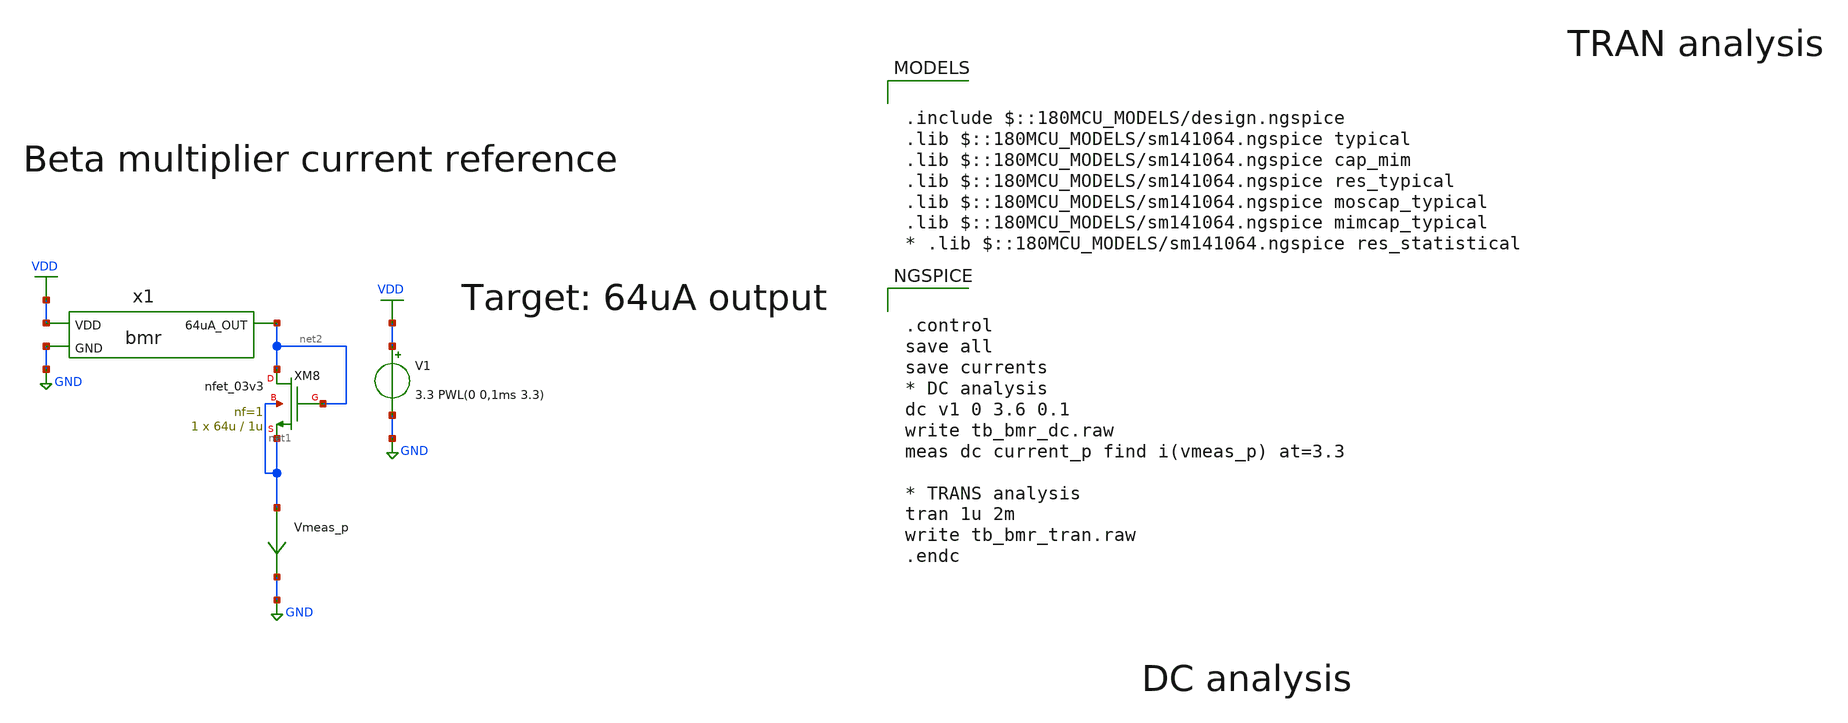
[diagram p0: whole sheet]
** sch_path: designs/libs/tb_analog/tb_bmr/tb_bmr.sch
* Copyright 2022 GlobalFoundries PDK Authors
* Licensed under the Apache License, Version 2.0 (the "License");
* you may not use this file except in compliance with the License.
* You may obtain a copy of the License at
* https://www.apache.org/licenses/LICENSE-2.0
* Unless required by applicable law or agreed to in writing, software
* distributed under the License is distributed on an "AS IS" BASIS,
* WITHOUT WARRANTIES OR CONDITIONS OF ANY KIND, either express or implied.
* See the License for the specific language governing permissions and
* limitations under the License.
**.subckt tb_bmr
V1 VDD GND 3.3 PWL(0 0,1ms 3.3)
Vmeas_p net1 GND 0
.save i(vmeas_p)
x1 VDD GND net2 bmr
XM8 net2 net2 net1 net1 nfet_03v3 L=1u W=64u nf=1 ad='int((nf+1)/2) * W/nf * 0.18u' as='int((nf+2)/2) * W/nf * 0.18u'
+ pd='2*int((nf+1)/2) * (W/nf + 0.18u)' ps='2*int((nf+2)/2) * (W/nf + 0.18u)' nrd='0.18u / W' nrs='0.18u / W'
+ sa=0 sb=0 sd=0 m=1
**** begin user architecture code


.control
save all
save currents
* DC analysis
dc v1 0 3.6 0.1
write tb_bmr_dc.raw
meas dc current_p find i(vmeas_p) at=3.3

* TRANS analysis
tran 1u 2m
write tb_bmr_tran.raw
.endc



.include $::180MCU_MODELS/design.ngspice
.lib $::180MCU_MODELS/sm141064.ngspice typical
.lib $::180MCU_MODELS/sm141064.ngspice cap_mim
.lib $::180MCU_MODELS/sm141064.ngspice res_typical
.lib $::180MCU_MODELS/sm141064.ngspice moscap_typical
.lib $::180MCU_MODELS/sm141064.ngspice mimcap_typical
* .lib $::180MCU_MODELS/sm141064.ngspice res_statistical

**** end user architecture code
**.ends

* expanding   symbol:  libs/core_analog/bmr/bmr.sym # of pins=3
** sym_path: designs/libs/core_analog/bmr/bmr.sym
** sch_path: designs/libs/core_analog/bmr/bmr.sch
.subckt bmr VDD GND 64uA_OUT
*.ipin VDD
*.ipin GND
*.opin 64uA_OUT
XM3 net2 net1 net3 GND nfet_03v3 L=1u W=10u nf=1 ad='int((nf+1)/2) * W/nf * 0.18u' as='int((nf+2)/2) * W/nf * 0.18u'
+ pd='2*int((nf+1)/2) * (W/nf + 0.18u)' ps='2*int((nf+2)/2) * (W/nf + 0.18u)' nrd='0.18u / W' nrs='0.18u / W'
+ sa=0 sb=0 sd=0 m=1
XM5 net3 net2 VDD VDD pfet_03v3 L=3u W=15u nf=1 ad='int((nf+1)/2) * W/nf * 0.18u' as='int((nf+2)/2) * W/nf * 0.18u'
+ pd='2*int((nf+1)/2) * (W/nf + 0.18u)' ps='2*int((nf+2)/2) * (W/nf + 0.18u)' nrd='0.18u / W' nrs='0.18u / W'
+ sa=0 sb=0 sd=0 m=1
XM6 net1 net1 VDD VDD pfet_03v3 L=4u W=4u nf=1 ad='int((nf+1)/2) * W/nf * 0.18u' as='int((nf+2)/2) * W/nf * 0.18u'
+ pd='2*int((nf+1)/2) * (W/nf + 0.18u)' ps='2*int((nf+2)/2) * (W/nf + 0.18u)' nrd='0.18u / W' nrs='0.18u / W'
+ sa=0 sb=0 sd=0 m=1
XM9 net2 net3 net4 net4 nfet_03v3 L=3u W=10u nf=1 ad='int((nf+1)/2) * W/nf * 0.18u' as='int((nf+2)/2) * W/nf * 0.18u'
+ pd='2*int((nf+1)/2) * (W/nf + 0.18u)' ps='2*int((nf+2)/2) * (W/nf + 0.18u)' nrd='0.18u / W' nrs='0.18u / W'
+ sa=0 sb=0 sd=0 m=1
XM12 net2 net2 VDD VDD pfet_03v3 L=3u W=15u nf=1 ad='int((nf+1)/2) * W/nf * 0.18u' as='int((nf+2)/2) * W/nf * 0.18u'
+ pd='2*int((nf+1)/2) * (W/nf + 0.18u)' ps='2*int((nf+2)/2) * (W/nf + 0.18u)' nrd='0.18u / W' nrs='0.18u / W'
+ sa=0 sb=0 sd=0 m=1
XM1 net1 net3 GND GND nfet_03v3 L=3u W=10u nf=1 ad='int((nf+1)/2) * W/nf * 0.18u' as='int((nf+2)/2) * W/nf * 0.18u'
+ pd='2*int((nf+1)/2) * (W/nf + 0.18u)' ps='2*int((nf+2)/2) * (W/nf + 0.18u)' nrd='0.18u / W' nrs='0.18u / W'
+ sa=0 sb=0 sd=0 m=1
XM2 net3 net3 GND GND nfet_03v3 L=3u W=5u nf=1 ad='int((nf+1)/2) * W/nf * 0.18u' as='int((nf+2)/2) * W/nf * 0.18u'
+ pd='2*int((nf+1)/2) * (W/nf + 0.18u)' ps='2*int((nf+2)/2) * (W/nf + 0.18u)' nrd='0.18u / W' nrs='0.18u / W'
+ sa=0 sb=0 sd=0 m=1
XM4 64uA_OUT net2 VDD VDD pfet_03v3 L=3u W=14u nf=1 ad='int((nf+1)/2) * W/nf * 0.18u' as='int((nf+2)/2) * W/nf * 0.18u'
+ pd='2*int((nf+1)/2) * (W/nf + 0.18u)' ps='2*int((nf+2)/2) * (W/nf + 0.18u)' nrd='0.18u / W' nrs='0.18u / W'
+ sa=0 sb=0 sd=0 m=1
XR1 GND net4 VDD ppolyf_u_3k r_width=1e-6 r_length=1e-6 m=1
.ends

.GLOBAL VDD
.GLOBAL GND
.end
